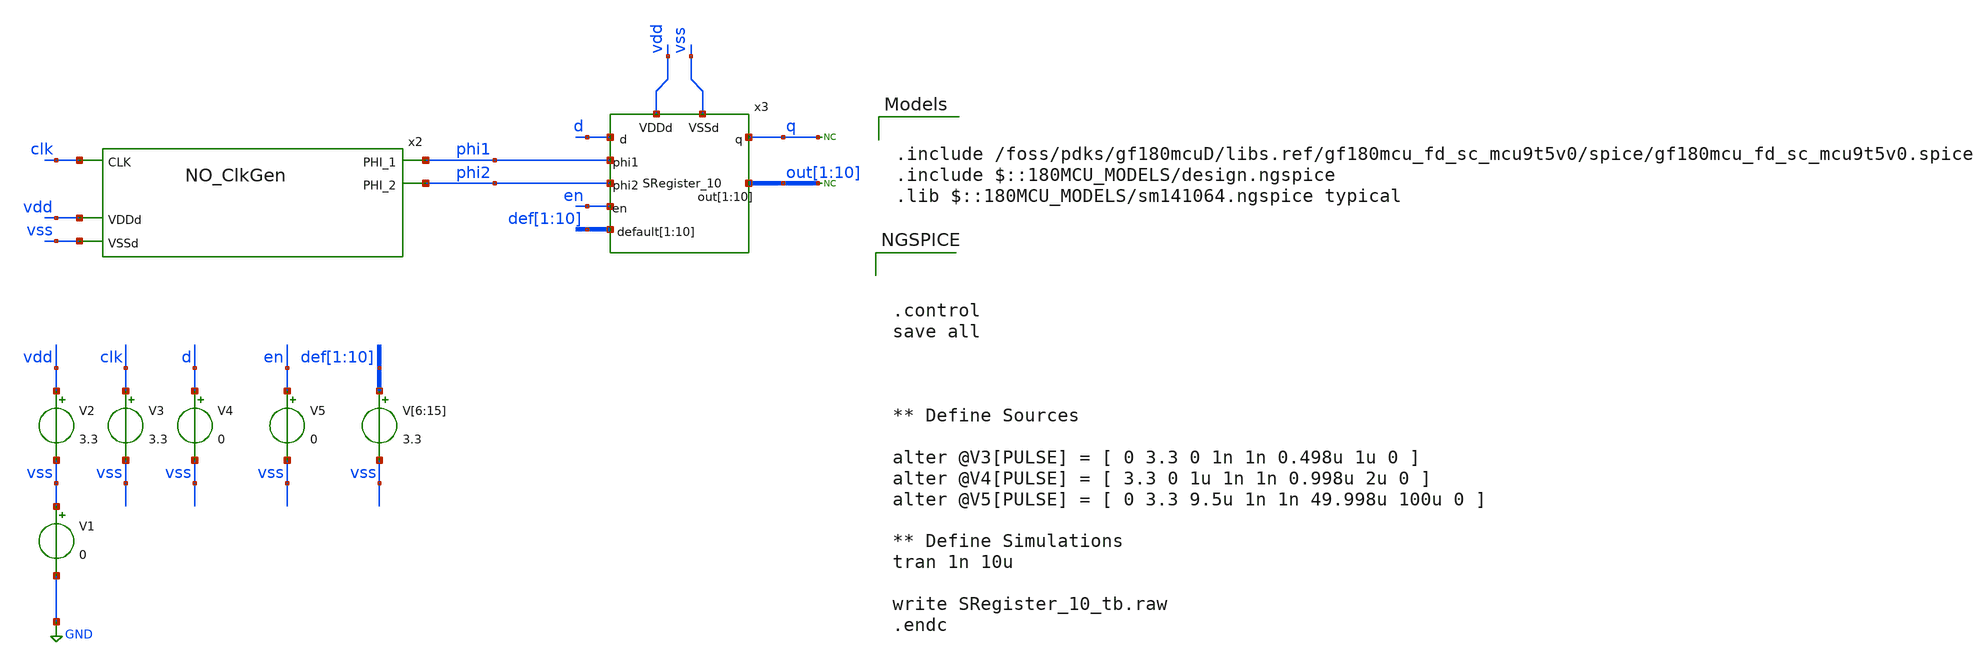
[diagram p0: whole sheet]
** sch_path: designs/libs/qw_tb_analog/SRegister_10_tb/SRegister_10_tb.sch
**.subckt SRegister_10_tb
V1 vss GND 0
V2 vdd vss 3.3
x2 phi2 clk phi1 vdd vss NO_ClkGen
V3 clk vss 3.3
V4 d vss 0
* noconn out[1:10]
V5 en vss 0
V[6] def[1] vss 3.3
V[7] def[2] vss 3.3
V[8] def[3] vss 3.3
V[9] def[4] vss 3.3
V[10] def[5] vss 3.3
V[11] def[6] vss 3.3
V[12] def[7] vss 3.3
V[13] def[8] vss 3.3
V[14] def[9] vss 3.3
V[15] def[10] vss 3.3
* noconn q
x3 vdd vss phi1 phi2 en def[1] def[2] def[3] def[4] def[5] def[6] def[7] def[8] def[9] def[10] d q
+ out[1] out[2] out[3] out[4] out[5] out[6] out[7] out[8] out[9] out[10] SRegister_10
**** begin user architecture code

.include /foss/pdks/gf180mcuD/libs.ref/gf180mcu_fd_sc_mcu9t5v0/spice/gf180mcu_fd_sc_mcu9t5v0.spice
.include $::180MCU_MODELS/design.ngspice
.lib $::180MCU_MODELS/sm141064.ngspice typical




.control
save all



** Define Sources

alter @V3[PULSE] = [ 0 3.3 0 1n 1n 0.498u 1u 0 ]
alter @V4[PULSE] = [ 3.3 0 1u 1n 1n 0.998u 2u 0 ]
alter @V5[PULSE] = [ 0 3.3 9.5u 1n 1n 49.998u 100u 0 ]

** Define Simulations
tran 1n 10u

write SRegister_10_tb.raw
.endc


**** end user architecture code
**.ends
.GLOBAL GND
.end
